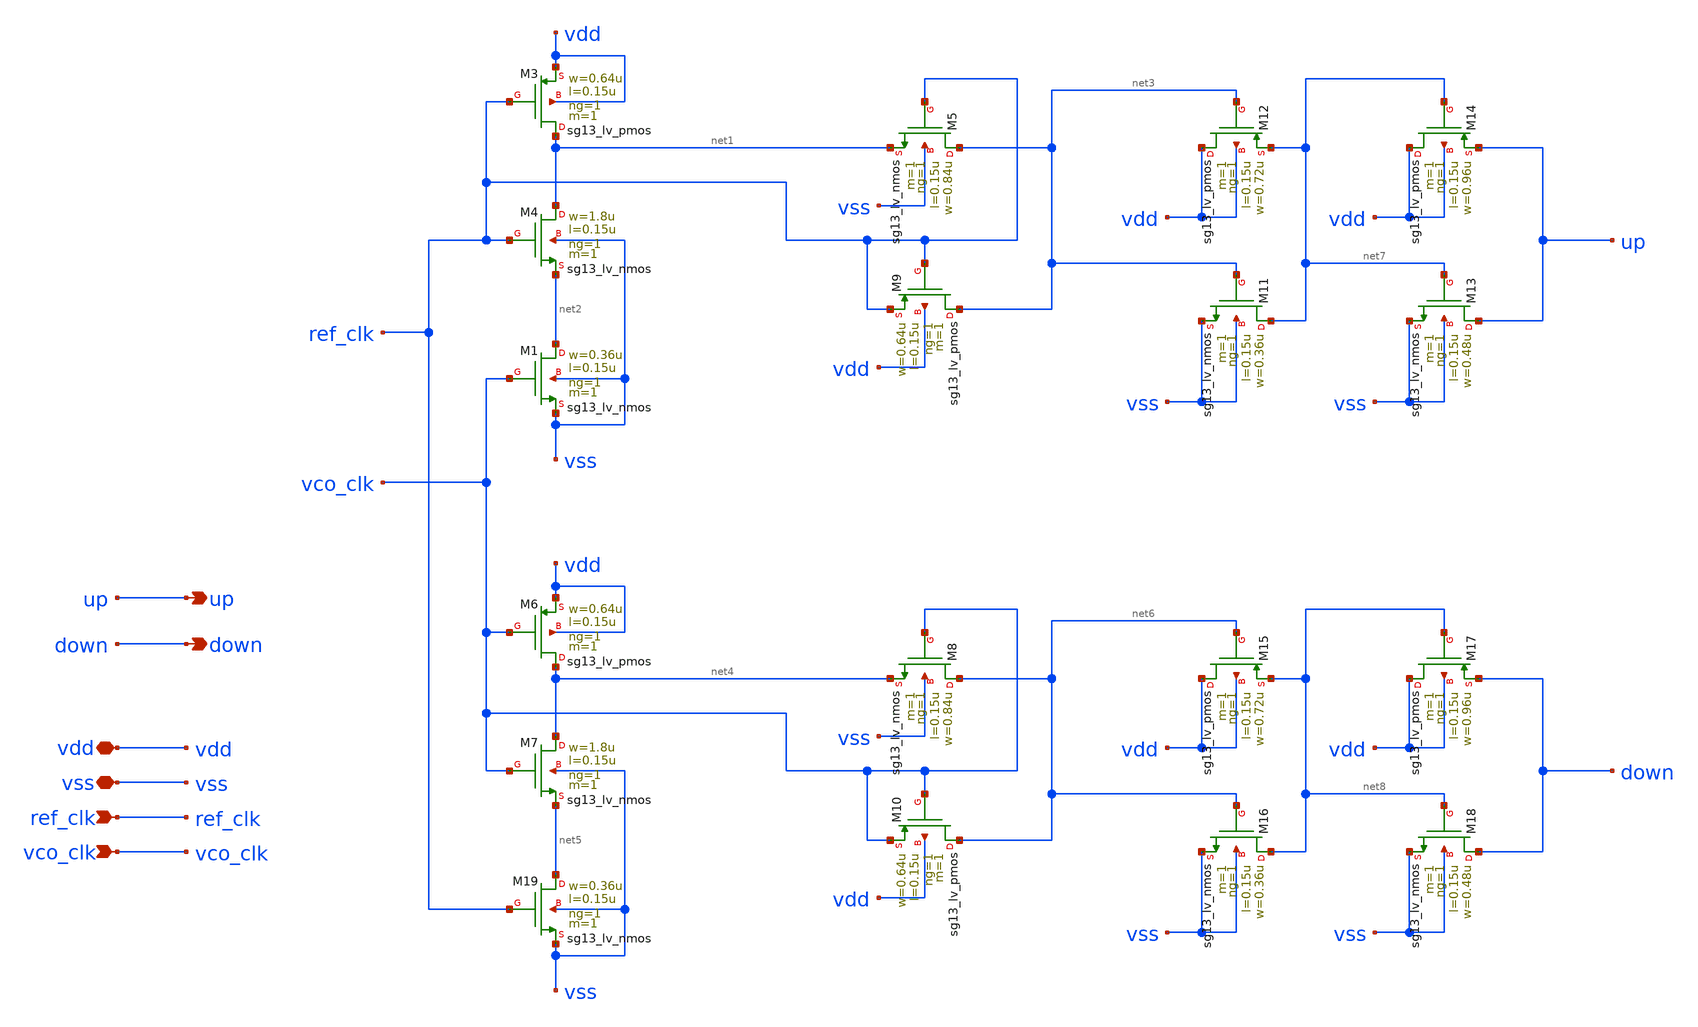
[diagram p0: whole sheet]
** sch_path: 30_MHz_Fractional_N_PLL/design_data/xschem/PFD.sch
**.subckt PFD vdd ref_clk vss vco_clk up down
*.iopin vdd
*.ipin ref_clk
*.iopin vss
*.ipin vco_clk
*.opin up
*.opin down
XM1 net2 vco_clk vss vss sg13_lv_nmos w=0.36u l=0.15u ng=1 m=1 mm_ok=1
XM4 net1 ref_clk net2 vss sg13_lv_nmos w=1.8u l=0.15u ng=1 m=1 mm_ok=1
XM5 net3 ref_clk net1 vss sg13_lv_nmos w=0.84u l=0.15u ng=1 m=1 mm_ok=1
XM9 net3 ref_clk ref_clk vdd sg13_lv_pmos w=0.64u l=0.15u ng=1 m=1 mm_ok=1
XM11 net7 net3 vss vss sg13_lv_nmos w=0.36u l=0.15u ng=1 m=1 mm_ok=1
XM12 vdd net3 net7 vdd sg13_lv_pmos w=0.72u l=0.15u ng=1 m=1 mm_ok=1
XM13 up net7 vss vss sg13_lv_nmos w=0.48u l=0.15u ng=1 m=1 mm_ok=1
XM14 vdd net7 up vdd sg13_lv_pmos w=0.96u l=0.15u ng=1 m=1 mm_ok=1
XM3 net1 ref_clk vdd vdd sg13_lv_pmos w=0.64u l=0.15u ng=1 m=1 mm_ok=1
XM6 net4 vco_clk vdd vdd sg13_lv_pmos w=0.64u l=0.15u ng=1 m=1 mm_ok=1
XM7 net4 vco_clk net5 vss sg13_lv_nmos w=1.8u l=0.15u ng=1 m=1 mm_ok=1
XM19 net5 ref_clk vss vss sg13_lv_nmos w=0.36u l=0.15u ng=1 m=1 mm_ok=1
XM8 net6 vco_clk net4 vss sg13_lv_nmos w=0.84u l=0.15u ng=1 m=1 mm_ok=1
XM10 net6 vco_clk vco_clk vdd sg13_lv_pmos w=0.64u l=0.15u ng=1 m=1 mm_ok=1
XM15 vdd net6 net8 vdd sg13_lv_pmos w=0.72u l=0.15u ng=1 m=1 mm_ok=1
XM16 net8 net6 vss vss sg13_lv_nmos w=0.36u l=0.15u ng=1 m=1 mm_ok=1
XM17 vdd net8 down vdd sg13_lv_pmos w=0.96u l=0.15u ng=1 m=1 mm_ok=1
XM18 down net8 vss vss sg13_lv_nmos w=0.48u l=0.15u ng=1 m=1 mm_ok=1
**.ends
.end
